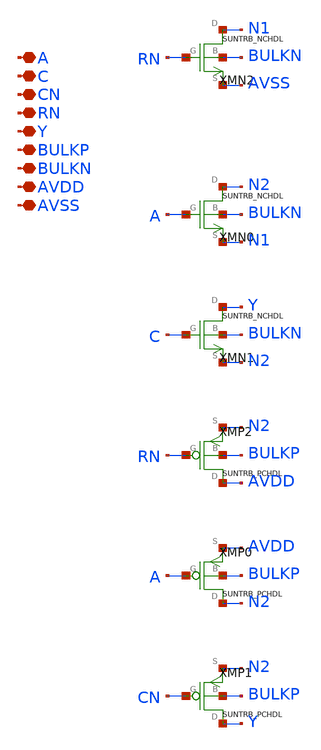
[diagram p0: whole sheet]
** sch_path: ip/sun_trb_sky130nm/design/SUN_TRB_SKY130NM/SUNTRB_NDTRIX1_CV.sch
**.subckt SUNTRB_NDTRIX1_CV A C CN RN Y BULKP BULKN AVDD AVSS
*.iopin A
*.iopin C
*.iopin CN
*.iopin RN
*.iopin Y
*.iopin BULKP
*.iopin BULKN
*.iopin AVDD
*.iopin AVSS
XMN2 N1 RN AVSS BULKN SUNTRB_NCHDL xoffset=0 yoffset=0 angle=0
XMN0 N2 A N1 BULKN SUNTRB_NCHDL xoffset=0 yoffset=0 angle=0
XMN1 Y C N2 BULKN SUNTRB_NCHDL xoffset=0 yoffset=0 angle=0
XMP2 AVDD RN N2 BULKP SUNTRB_PCHDL xoffset=0 yoffset=0 angle=0
XMP0 N2 A AVDD BULKP SUNTRB_PCHDL xoffset=0 yoffset=0 angle=0
XMP1 Y CN N2 BULKP SUNTRB_PCHDL xoffset=0 yoffset=0 angle=0
**.ends
.end
